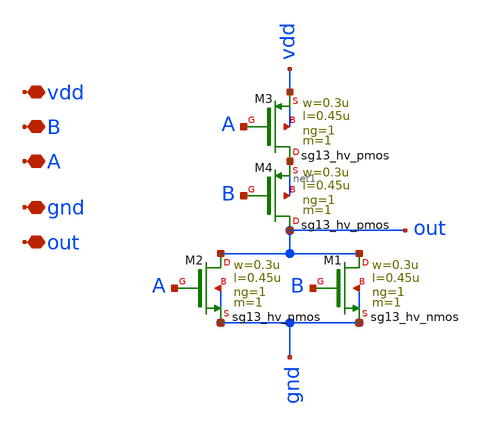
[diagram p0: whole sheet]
** sch_path: Clock_gen_using_transistor_hv/nor.sch
**.subckt nor vdd B A gnd out
*.iopin vdd
*.iopin B
*.iopin A
*.iopin gnd
*.iopin out
XM3 net1 A vdd vdd sg13_hv_pmos w=0.3u l=0.45u ng=1 m=1 mm_ok=1
XM1 out B gnd gnd sg13_hv_nmos w=0.3u l=0.45u ng=1 m=1 mm_ok=1
XM2 out A gnd gnd sg13_hv_nmos w=0.3u l=0.45u ng=1 m=1 mm_ok=1
XM4 out B net1 net1 sg13_hv_pmos w=0.3u l=0.45u ng=1 m=1 mm_ok=1
**.ends
.end
